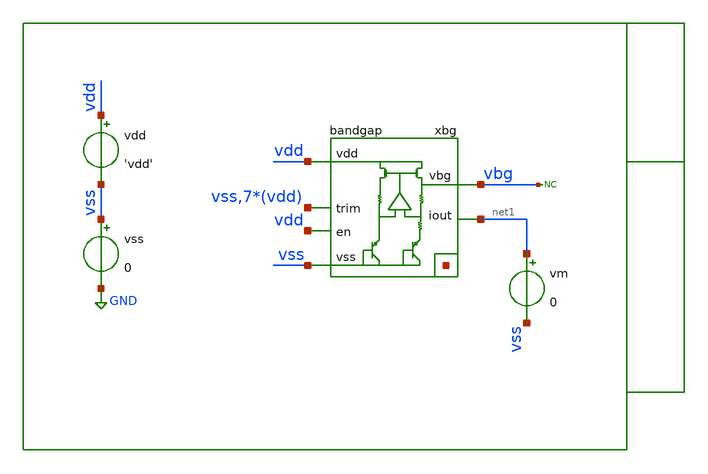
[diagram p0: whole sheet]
** sch_path: xschem/tb/bandgap_cm/bandgap/op_bandgap.sch
**.subckt op_bandgap
xbg vdd vbg vss net2[7] net2[6] net2[5] net2[4] net2[3] net2[2] net2[1] net2[0] vss vdd vdd vdd vdd
+ vdd vdd vdd net1 vdd bandgap
vdd vdd vss 'vdd'
vss vss GND 0
* noconn vbg
vm net1 vss 0
**** begin user architecture code

* Control

.param vdd = 3.3

.temp = 27

.options reltol  = 1e-6
.options abstol  = 1e-12
.options gmin    = 1e-15

*------------------------------------------------------------
* Nodeset for better convergence
*------------------------------------------------------------
.nodeset v(vbg)  = '1'
.nodeset v(xbg.gate) = 'vdd/2'
.nodeset v(xbg.vx)   = '0.70'
.nodeset v(xbg.vbe2) = '0.65'
.nodeset v(xbg.vs1)  = '0'
*------------------------------------------------------------


.control

save all

* optran 0 0 0 100n 0.3m 0
op

let gm_xbg_xm2 = @m.xbg.xm2.m0[gm]
let gm_xbg_xms1 = @m.xbg.xms1.m0[gm]
let gm_xbg_xm1 = @m.xbg.xm1.m0[gm]
let gm_xbg_xmo1 = @m.xbg.xmo1.m0[gm]
let gm_xbg_xmb1 = @m.xbg.xmb1.m0[gm]
let gm_xbg_xmb2 = @m.xbg.xmb2.m0[gm]
let gm_xbg_xmb3 = @m.xbg.xmb3.m0[gm]
let gm_xbg_xmb2 = @m.xbg.xmb2.m0[gm]
let gm_xbg_xmb3 = @m.xbg.xmb3.m0[gm]
let gm_xbg_xmo2 = @m.xbg.xmo2.m0[gm]
let gm_xbg_xme1 = @m.xbg.xme1.m0[gm]
let gm_xbg_xme2 = @m.xbg.xme2.m0[gm]
let gm_xbg_xmi2 = @m.xbg.xmi2.m0[gm]
let gm_xbg_xmi1 = @m.xbg.xmi1.m0[gm]
let gm_xbg_xme3 = @m.xbg.xme3.m0[gm]
let gm_xbg_xme4 = @m.xbg.xme4.m0[gm]
let gm_xbg_xms2 = @m.xbg.xms2.m0[gm]
let gm_xbg_xms3 = @m.xbg.xms3.m0[gm]
let gm_xbg_xms4 = @m.xbg.xms4.m0[gm]
let gm_xamp_xmb1 = @m.xbg.xamp.xmb1.m0[gm]
let gm_xamp_xmb3 = @m.xbg.xamp.xmb3.m0[gm]
let gm_xamp_xmb2 = @m.xbg.xamp.xmb2.m0[gm]
let gm_xamp_xmd1 = @m.xbg.xamp.xmd1.m0[gm]
let gm_xamp_xmb4 = @m.xbg.xamp.xmb4.m0[gm]
let gm_xamp_xmb5 = @m.xbg.xamp.xmb5.m0[gm]
let gm_xamp_xmd2 = @m.xbg.xamp.xmd2.m0[gm]
let gm_xamp_xmt1 = @m.xbg.xamp.xmt1.m0[gm]
let gm_xamp_xmc7 = @m.xbg.xamp.xmc7.m0[gm]
let gm_xamp_xmc8 = @m.xbg.xamp.xmc8.m0[gm]
let gm_xamp_xmc1 = @m.xbg.xamp.xmc1.m0[gm]
let gm_xamp_xmc2 = @m.xbg.xamp.xmc2.m0[gm]
let gm_xamp_xmc3 = @m.xbg.xamp.xmc3.m0[gm]
let gm_xamp_xmc4 = @m.xbg.xamp.xmc4.m0[gm]
let gm_xamp_xmc5 = @m.xbg.xamp.xmc5.m0[gm]
let gm_xamp_xmc6 = @m.xbg.xamp.xmc6.m0[gm]
let gds_xbg_xm2 = @m.xbg.xm2.m0[gds]
let gds_xbg_xms1 = @m.xbg.xms1.m0[gds]
let gds_xbg_xm1 = @m.xbg.xm1.m0[gds]
let gds_xbg_xmo1 = @m.xbg.xmo1.m0[gds]
let gds_xbg_xmb1 = @m.xbg.xmb1.m0[gds]
let gds_xbg_xmb2 = @m.xbg.xmb2.m0[gds]
let gds_xbg_xmb3 = @m.xbg.xmb3.m0[gds]
let gds_xbg_xmb2 = @m.xbg.xmb2.m0[gds]
let gds_xbg_xmb3 = @m.xbg.xmb3.m0[gds]
let gds_xbg_xmo2 = @m.xbg.xmo2.m0[gds]
let gds_xbg_xme1 = @m.xbg.xme1.m0[gds]
let gds_xbg_xme2 = @m.xbg.xme2.m0[gds]
let gds_xbg_xmi2 = @m.xbg.xmi2.m0[gds]
let gds_xbg_xmi1 = @m.xbg.xmi1.m0[gds]
let gds_xbg_xme3 = @m.xbg.xme3.m0[gds]
let gds_xbg_xme4 = @m.xbg.xme4.m0[gds]
let gds_xbg_xms2 = @m.xbg.xms2.m0[gds]
let gds_xbg_xms3 = @m.xbg.xms3.m0[gds]
let gds_xbg_xms4 = @m.xbg.xms4.m0[gds]
let gds_xamp_xmb1 = @m.xbg.xamp.xmb1.m0[gds]
let gds_xamp_xmb3 = @m.xbg.xamp.xmb3.m0[gds]
let gds_xamp_xmb2 = @m.xbg.xamp.xmb2.m0[gds]
let gds_xamp_xmd1 = @m.xbg.xamp.xmd1.m0[gds]
let gds_xamp_xmb4 = @m.xbg.xamp.xmb4.m0[gds]
let gds_xamp_xmb5 = @m.xbg.xamp.xmb5.m0[gds]
let gds_xamp_xmd2 = @m.xbg.xamp.xmd2.m0[gds]
let gds_xamp_xmt1 = @m.xbg.xamp.xmt1.m0[gds]
let gds_xamp_xmc7 = @m.xbg.xamp.xmc7.m0[gds]
let gds_xamp_xmc8 = @m.xbg.xamp.xmc8.m0[gds]
let gds_xamp_xmc1 = @m.xbg.xamp.xmc1.m0[gds]
let gds_xamp_xmc2 = @m.xbg.xamp.xmc2.m0[gds]
let gds_xamp_xmc3 = @m.xbg.xamp.xmc3.m0[gds]
let gds_xamp_xmc4 = @m.xbg.xamp.xmc4.m0[gds]
let gds_xamp_xmc5 = @m.xbg.xamp.xmc5.m0[gds]
let gds_xamp_xmc6 = @m.xbg.xamp.xmc6.m0[gds]
let vdsat_xbg_xm2 = @m.xbg.xm2.m0[vdsat]
let vdsat_xbg_xms1 = @m.xbg.xms1.m0[vdsat]
let vdsat_xbg_xm1 = @m.xbg.xm1.m0[vdsat]
let vdsat_xbg_xmo1 = @m.xbg.xmo1.m0[vdsat]
let vdsat_xbg_xmb1 = @m.xbg.xmb1.m0[vdsat]
let vdsat_xbg_xmb2 = @m.xbg.xmb2.m0[vdsat]
let vdsat_xbg_xmb3 = @m.xbg.xmb3.m0[vdsat]
let vdsat_xbg_xmb2 = @m.xbg.xmb2.m0[vdsat]
let vdsat_xbg_xmb3 = @m.xbg.xmb3.m0[vdsat]
let vdsat_xbg_xmo2 = @m.xbg.xmo2.m0[vdsat]
let vdsat_xbg_xme1 = @m.xbg.xme1.m0[vdsat]
let vdsat_xbg_xme2 = @m.xbg.xme2.m0[vdsat]
let vdsat_xbg_xmi2 = @m.xbg.xmi2.m0[vdsat]
let vdsat_xbg_xmi1 = @m.xbg.xmi1.m0[vdsat]
let vdsat_xbg_xme3 = @m.xbg.xme3.m0[vdsat]
let vdsat_xbg_xme4 = @m.xbg.xme4.m0[vdsat]
let vdsat_xbg_xms2 = @m.xbg.xms2.m0[vdsat]
let vdsat_xbg_xms3 = @m.xbg.xms3.m0[vdsat]
let vdsat_xbg_xms4 = @m.xbg.xms4.m0[vdsat]
let vdsat_xamp_xmb1 = @m.xbg.xamp.xmb1.m0[vdsat]
let vdsat_xamp_xmb3 = @m.xbg.xamp.xmb3.m0[vdsat]
let vdsat_xamp_xmb2 = @m.xbg.xamp.xmb2.m0[vdsat]
let vdsat_xamp_xmd1 = @m.xbg.xamp.xmd1.m0[vdsat]
let vdsat_xamp_xmb4 = @m.xbg.xamp.xmb4.m0[vdsat]
let vdsat_xamp_xmb5 = @m.xbg.xamp.xmb5.m0[vdsat]
let vdsat_xamp_xmd2 = @m.xbg.xamp.xmd2.m0[vdsat]
let vdsat_xamp_xmt1 = @m.xbg.xamp.xmt1.m0[vdsat]
let vdsat_xamp_xmc7 = @m.xbg.xamp.xmc7.m0[vdsat]
let vdsat_xamp_xmc8 = @m.xbg.xamp.xmc8.m0[vdsat]
let vdsat_xamp_xmc1 = @m.xbg.xamp.xmc1.m0[vdsat]
let vdsat_xamp_xmc2 = @m.xbg.xamp.xmc2.m0[vdsat]
let vdsat_xamp_xmc3 = @m.xbg.xamp.xmc3.m0[vdsat]
let vdsat_xamp_xmc4 = @m.xbg.xamp.xmc4.m0[vdsat]
let vdsat_xamp_xmc5 = @m.xbg.xamp.xmc5.m0[vdsat]
let vdsat_xamp_xmc6 = @m.xbg.xamp.xmc6.m0[vdsat]
let vth_xbg_xm2 = @m.xbg.xm2.m0[vth]
let vth_xbg_xms1 = @m.xbg.xms1.m0[vth]
let vth_xbg_xm1 = @m.xbg.xm1.m0[vth]
let vth_xbg_xmo1 = @m.xbg.xmo1.m0[vth]
let vth_xbg_xmb1 = @m.xbg.xmb1.m0[vth]
let vth_xbg_xmb2 = @m.xbg.xmb2.m0[vth]
let vth_xbg_xmb3 = @m.xbg.xmb3.m0[vth]
let vth_xbg_xmb2 = @m.xbg.xmb2.m0[vth]
let vth_xbg_xmb3 = @m.xbg.xmb3.m0[vth]
let vth_xbg_xmo2 = @m.xbg.xmo2.m0[vth]
let vth_xbg_xme1 = @m.xbg.xme1.m0[vth]
let vth_xbg_xme2 = @m.xbg.xme2.m0[vth]
let vth_xbg_xmi2 = @m.xbg.xmi2.m0[vth]
let vth_xbg_xmi1 = @m.xbg.xmi1.m0[vth]
let vth_xbg_xme3 = @m.xbg.xme3.m0[vth]
let vth_xbg_xme4 = @m.xbg.xme4.m0[vth]
let vth_xbg_xms2 = @m.xbg.xms2.m0[vth]
let vth_xbg_xms3 = @m.xbg.xms3.m0[vth]
let vth_xbg_xms4 = @m.xbg.xms4.m0[vth]
let vth_xamp_xmb1 = @m.xbg.xamp.xmb1.m0[vth]
let vth_xamp_xmb3 = @m.xbg.xamp.xmb3.m0[vth]
let vth_xamp_xmb2 = @m.xbg.xamp.xmb2.m0[vth]
let vth_xamp_xmd1 = @m.xbg.xamp.xmd1.m0[vth]
let vth_xamp_xmb4 = @m.xbg.xamp.xmb4.m0[vth]
let vth_xamp_xmb5 = @m.xbg.xamp.xmb5.m0[vth]
let vth_xamp_xmd2 = @m.xbg.xamp.xmd2.m0[vth]
let vth_xamp_xmt1 = @m.xbg.xamp.xmt1.m0[vth]
let vth_xamp_xmc7 = @m.xbg.xamp.xmc7.m0[vth]
let vth_xamp_xmc8 = @m.xbg.xamp.xmc8.m0[vth]
let vth_xamp_xmc1 = @m.xbg.xamp.xmc1.m0[vth]
let vth_xamp_xmc2 = @m.xbg.xamp.xmc2.m0[vth]
let vth_xamp_xmc3 = @m.xbg.xamp.xmc3.m0[vth]
let vth_xamp_xmc4 = @m.xbg.xamp.xmc4.m0[vth]
let vth_xamp_xmc5 = @m.xbg.xamp.xmc5.m0[vth]
let vth_xamp_xmc6 = @m.xbg.xamp.xmc6.m0[vth]
let id_xbg_xm2 = @m.xbg.xm2.m0[id]
let id_xbg_xms1 = @m.xbg.xms1.m0[id]
let id_xbg_xm1 = @m.xbg.xm1.m0[id]
let id_xbg_xmo1 = @m.xbg.xmo1.m0[id]
let id_xbg_xmb1 = @m.xbg.xmb1.m0[id]
let id_xbg_xmb2 = @m.xbg.xmb2.m0[id]
let id_xbg_xmb3 = @m.xbg.xmb3.m0[id]
let id_xbg_xmb2 = @m.xbg.xmb2.m0[id]
let id_xbg_xmb3 = @m.xbg.xmb3.m0[id]
let id_xbg_xmo2 = @m.xbg.xmo2.m0[id]
let id_xbg_xme1 = @m.xbg.xme1.m0[id]
let id_xbg_xme2 = @m.xbg.xme2.m0[id]
let id_xbg_xmi2 = @m.xbg.xmi2.m0[id]
let id_xbg_xmi1 = @m.xbg.xmi1.m0[id]
let id_xbg_xme3 = @m.xbg.xme3.m0[id]
let id_xbg_xme4 = @m.xbg.xme4.m0[id]
let id_xbg_xms2 = @m.xbg.xms2.m0[id]
let id_xbg_xms3 = @m.xbg.xms3.m0[id]
let id_xbg_xms4 = @m.xbg.xms4.m0[id]
let id_xamp_xmb1 = @m.xbg.xamp.xmb1.m0[id]
let id_xamp_xmb3 = @m.xbg.xamp.xmb3.m0[id]
let id_xamp_xmb2 = @m.xbg.xamp.xmb2.m0[id]
let id_xamp_xmd1 = @m.xbg.xamp.xmd1.m0[id]
let id_xamp_xmb4 = @m.xbg.xamp.xmb4.m0[id]
let id_xamp_xmb5 = @m.xbg.xamp.xmb5.m0[id]
let id_xamp_xmd2 = @m.xbg.xamp.xmd2.m0[id]
let id_xamp_xmt1 = @m.xbg.xamp.xmt1.m0[id]
let id_xamp_xmc7 = @m.xbg.xamp.xmc7.m0[id]
let id_xamp_xmc8 = @m.xbg.xamp.xmc8.m0[id]
let id_xamp_xmc1 = @m.xbg.xamp.xmc1.m0[id]
let id_xamp_xmc2 = @m.xbg.xamp.xmc2.m0[id]
let id_xamp_xmc3 = @m.xbg.xamp.xmc3.m0[id]
let id_xamp_xmc4 = @m.xbg.xamp.xmc4.m0[id]
let id_xamp_xmc5 = @m.xbg.xamp.xmc5.m0[id]
let id_xamp_xmc6 = @m.xbg.xamp.xmc6.m0[id]
let vgs_xbg_xm2 = @m.xbg.xm2.m0[vgs]
let vgs_xbg_xms1 = @m.xbg.xms1.m0[vgs]
let vgs_xbg_xm1 = @m.xbg.xm1.m0[vgs]
let vgs_xbg_xmo1 = @m.xbg.xmo1.m0[vgs]
let vgs_xbg_xmb1 = @m.xbg.xmb1.m0[vgs]
let vgs_xbg_xmb2 = @m.xbg.xmb2.m0[vgs]
let vgs_xbg_xmb3 = @m.xbg.xmb3.m0[vgs]
let vgs_xbg_xmb2 = @m.xbg.xmb2.m0[vgs]
let vgs_xbg_xmb3 = @m.xbg.xmb3.m0[vgs]
let vgs_xbg_xmo2 = @m.xbg.xmo2.m0[vgs]
let vgs_xbg_xme1 = @m.xbg.xme1.m0[vgs]
let vgs_xbg_xme2 = @m.xbg.xme2.m0[vgs]
let vgs_xbg_xmi2 = @m.xbg.xmi2.m0[vgs]
let vgs_xbg_xmi1 = @m.xbg.xmi1.m0[vgs]
let vgs_xbg_xme3 = @m.xbg.xme3.m0[vgs]
let vgs_xbg_xme4 = @m.xbg.xme4.m0[vgs]
let vgs_xbg_xms2 = @m.xbg.xms2.m0[vgs]
let vgs_xbg_xms3 = @m.xbg.xms3.m0[vgs]
let vgs_xbg_xms4 = @m.xbg.xms4.m0[vgs]
let vgs_xamp_xmb1 = @m.xbg.xamp.xmb1.m0[vgs]
let vgs_xamp_xmb3 = @m.xbg.xamp.xmb3.m0[vgs]
let vgs_xamp_xmb2 = @m.xbg.xamp.xmb2.m0[vgs]
let vgs_xamp_xmd1 = @m.xbg.xamp.xmd1.m0[vgs]
let vgs_xamp_xmb4 = @m.xbg.xamp.xmb4.m0[vgs]
let vgs_xamp_xmb5 = @m.xbg.xamp.xmb5.m0[vgs]
let vgs_xamp_xmd2 = @m.xbg.xamp.xmd2.m0[vgs]
let vgs_xamp_xmt1 = @m.xbg.xamp.xmt1.m0[vgs]
let vgs_xamp_xmc7 = @m.xbg.xamp.xmc7.m0[vgs]
let vgs_xamp_xmc8 = @m.xbg.xamp.xmc8.m0[vgs]
let vgs_xamp_xmc1 = @m.xbg.xamp.xmc1.m0[vgs]
let vgs_xamp_xmc2 = @m.xbg.xamp.xmc2.m0[vgs]
let vgs_xamp_xmc3 = @m.xbg.xamp.xmc3.m0[vgs]
let vgs_xamp_xmc4 = @m.xbg.xamp.xmc4.m0[vgs]
let vgs_xamp_xmc5 = @m.xbg.xamp.xmc5.m0[vgs]
let vgs_xamp_xmc6 = @m.xbg.xamp.xmc6.m0[vgs]
let vds_xbg_xm2 = @m.xbg.xm2.m0[vds]
let vds_xbg_xms1 = @m.xbg.xms1.m0[vds]
let vds_xbg_xm1 = @m.xbg.xm1.m0[vds]
let vds_xbg_xmo1 = @m.xbg.xmo1.m0[vds]
let vds_xbg_xmb1 = @m.xbg.xmb1.m0[vds]
let vds_xbg_xmb2 = @m.xbg.xmb2.m0[vds]
let vds_xbg_xmb3 = @m.xbg.xmb3.m0[vds]
let vds_xbg_xmb2 = @m.xbg.xmb2.m0[vds]
let vds_xbg_xmb3 = @m.xbg.xmb3.m0[vds]
let vds_xbg_xmo2 = @m.xbg.xmo2.m0[vds]
let vds_xbg_xme1 = @m.xbg.xme1.m0[vds]
let vds_xbg_xme2 = @m.xbg.xme2.m0[vds]
let vds_xbg_xmi2 = @m.xbg.xmi2.m0[vds]
let vds_xbg_xmi1 = @m.xbg.xmi1.m0[vds]
let vds_xbg_xme3 = @m.xbg.xme3.m0[vds]
let vds_xbg_xme4 = @m.xbg.xme4.m0[vds]
let vds_xbg_xms2 = @m.xbg.xms2.m0[vds]
let vds_xbg_xms3 = @m.xbg.xms3.m0[vds]
let vds_xbg_xms4 = @m.xbg.xms4.m0[vds]
let vds_xamp_xmb1 = @m.xbg.xamp.xmb1.m0[vds]
let vds_xamp_xmb3 = @m.xbg.xamp.xmb3.m0[vds]
let vds_xamp_xmb2 = @m.xbg.xamp.xmb2.m0[vds]
let vds_xamp_xmd1 = @m.xbg.xamp.xmd1.m0[vds]
let vds_xamp_xmb4 = @m.xbg.xamp.xmb4.m0[vds]
let vds_xamp_xmb5 = @m.xbg.xamp.xmb5.m0[vds]
let vds_xamp_xmd2 = @m.xbg.xamp.xmd2.m0[vds]
let vds_xamp_xmt1 = @m.xbg.xamp.xmt1.m0[vds]
let vds_xamp_xmc7 = @m.xbg.xamp.xmc7.m0[vds]
let vds_xamp_xmc8 = @m.xbg.xamp.xmc8.m0[vds]
let vds_xamp_xmc1 = @m.xbg.xamp.xmc1.m0[vds]
let vds_xamp_xmc2 = @m.xbg.xamp.xmc2.m0[vds]
let vds_xamp_xmc3 = @m.xbg.xamp.xmc3.m0[vds]
let vds_xamp_xmc4 = @m.xbg.xamp.xmc4.m0[vds]
let vds_xamp_xmc5 = @m.xbg.xamp.xmc5.m0[vds]
let vds_xamp_xmc6 = @m.xbg.xamp.xmc6.m0[vds]

let vsat_xbg_xm2  = vds_xbg_xm2  - vdsat_xbg_xm2
let vsat_xbg_xms1 = vds_xbg_xms1 - vdsat_xbg_xms1
let vsat_xbg_xm1  = vds_xbg_xm1  - vdsat_xbg_xm1
let vsat_xbg_xmo1 = vds_xbg_xmo1 - vdsat_xbg_xmo1
let vsat_xbg_xmb1 = vds_xbg_xmb1 - vdsat_xbg_xmb1
let vsat_xbg_xmb2 = vds_xbg_xmb2 - vdsat_xbg_xmb2
let vsat_xbg_xmb3 = vds_xbg_xmb3 - vdsat_xbg_xmb3
let vsat_xbg_xmb2 = vds_xbg_xmb2 - vdsat_xbg_xmb2
let vsat_xbg_xmb3 = vds_xbg_xmb3 - vdsat_xbg_xmb3
let vsat_xbg_xmo2 = vds_xbg_xmo2 - vdsat_xbg_xmo2
let vsat_xbg_xme1 = vds_xbg_xme1 - vdsat_xbg_xme1
let vsat_xbg_xme2 = vds_xbg_xme2 - vdsat_xbg_xme2
let vsat_xbg_xmi2 = vds_xbg_xmi2 - vdsat_xbg_xmi2
let vsat_xbg_xmi1 = vds_xbg_xmi1 - vdsat_xbg_xmi1
let vsat_xbg_xme3 = vds_xbg_xme3 - vdsat_xbg_xme3
let vsat_xbg_xme4 = vds_xbg_xme4 - vdsat_xbg_xme4
let vsat_xbg_xms2 = vds_xbg_xms2 - vdsat_xbg_xms2
let vsat_xbg_xms3 = vds_xbg_xms3 - vdsat_xbg_xms3
let vsat_xbg_xms4 = vds_xbg_xms4 - vdsat_xbg_xms4
let vsat_xamp_xmb1 = vds_xamp_xmb1 - vdsat_xamp_xmb1
let vsat_xamp_xmb3 = vds_xamp_xmb3 - vdsat_xamp_xmb3
let vsat_xamp_xmb2 = vds_xamp_xmb2 - vdsat_xamp_xmb2
let vsat_xamp_xmd1 = vds_xamp_xmd1 - vdsat_xamp_xmd1
let vsat_xamp_xmb4 = vds_xamp_xmb4 - vdsat_xamp_xmb4
let vsat_xamp_xmb5 = vds_xamp_xmb5 - vdsat_xamp_xmb5
let vsat_xamp_xmd2 = vds_xamp_xmd2 - vdsat_xamp_xmd2
let vsat_xamp_xmt1 = vds_xamp_xmt1 - vdsat_xamp_xmt1
let vsat_xamp_xmc7 = vds_xamp_xmc7 - vdsat_xamp_xmc7
let vsat_xamp_xmc8 = vds_xamp_xmc8 - vdsat_xamp_xmc8
let vsat_xamp_xmc1 = vds_xamp_xmc1 - vdsat_xamp_xmc1
let vsat_xamp_xmc2 = vds_xamp_xmc2 - vdsat_xamp_xmc2
let vsat_xamp_xmc3 = vds_xamp_xmc3 - vdsat_xamp_xmc3
let vsat_xamp_xmc4 = vds_xamp_xmc4 - vdsat_xamp_xmc4
let vsat_xamp_xmc5 = vds_xamp_xmc5 - vdsat_xamp_xmc5
let vsat_xamp_xmc6 = vds_xamp_xmc6 - vdsat_xamp_xmc6

let vov_xbg_xm2  = vgs_xbg_xm2  - vth_xbg_xm2
let vov_xbg_xms1 = vgs_xbg_xms1 - vth_xbg_xms1
let vov_xbg_xm1  = vgs_xbg_xm1  - vth_xbg_xm1
let vov_xbg_xmo1 = vgs_xbg_xmo1 - vth_xbg_xmo1
let vov_xbg_xmb1 = vgs_xbg_xmb1 - vth_xbg_xmb1
let vov_xbg_xmb2 = vgs_xbg_xmb2 - vth_xbg_xmb2
let vov_xbg_xmb3 = vgs_xbg_xmb3 - vth_xbg_xmb3
let vov_xbg_xmb2 = vgs_xbg_xmb2 - vth_xbg_xmb2
let vov_xbg_xmb3 = vgs_xbg_xmb3 - vth_xbg_xmb3
let vov_xbg_xmo2 = vgs_xbg_xmo2 - vth_xbg_xmo2
let vov_xbg_xme1 = vgs_xbg_xme1 - vth_xbg_xme1
let vov_xbg_xme2 = vgs_xbg_xme2 - vth_xbg_xme2
let vov_xbg_xmi2 = vgs_xbg_xmi2 - vth_xbg_xmi2
let vov_xbg_xmi1 = vgs_xbg_xmi1 - vth_xbg_xmi1
let vov_xbg_xme3 = vgs_xbg_xme3 - vth_xbg_xme3
let vov_xbg_xme4 = vgs_xbg_xme4 - vth_xbg_xme4
let vov_xbg_xms2 = vgs_xbg_xms2 - vth_xbg_xms2
let vov_xbg_xms3 = vgs_xbg_xms3 - vth_xbg_xms3
let vov_xbg_xms4 = vgs_xbg_xms4 - vth_xbg_xms4
let vov_xamp_xmb1 = vgs_xamp_xmb1 - vth_xamp_xmb1
let vov_xamp_xmb3 = vgs_xamp_xmb3 - vth_xamp_xmb3
let vov_xamp_xmb2 = vgs_xamp_xmb2 - vth_xamp_xmb2
let vov_xamp_xmd1 = vgs_xamp_xmd1 - vth_xamp_xmd1
let vov_xamp_xmb4 = vgs_xamp_xmb4 - vth_xamp_xmb4
let vov_xamp_xmb5 = vgs_xamp_xmb5 - vth_xamp_xmb5
let vov_xamp_xmd2 = vgs_xamp_xmd2 - vth_xamp_xmd2
let vov_xamp_xmt1 = vgs_xamp_xmt1 - vth_xamp_xmt1
let vov_xamp_xmc7 = vgs_xamp_xmc7 - vth_xamp_xmc7
let vov_xamp_xmc8 = vgs_xamp_xmc8 - vth_xamp_xmc8
let vov_xamp_xmc1 = vgs_xamp_xmc1 - vth_xamp_xmc1
let vov_xamp_xmc2 = vgs_xamp_xmc2 - vth_xamp_xmc2
let vov_xamp_xmc3 = vgs_xamp_xmc3 - vth_xamp_xmc3
let vov_xamp_xmc4 = vgs_xamp_xmc4 - vth_xamp_xmc4
let vov_xamp_xmc5 = vgs_xamp_xmc5 - vth_xamp_xmc5
let vov_xamp_xmc6 = vgs_xamp_xmc6 - vth_xamp_xmc6



let ie_xq1 = abs(v.xbg.vmbjt1#branch)
let ie_xq2 = abs(v.xbg.vmbjt2#branch)
let i_amp = abs(v.xbg.vmamp#branch)
let i_xm1 = abs(v.xbg.vmxm1#branch)
let i_xm2 = abs(v.xbg.vmxm2#branch)
let i_r1 = ie_xq2
let i_r3 = abs(v.xbg.vmr3#branch)
let i_r2 = abs(v.xbg.vmr2#branch)
let iout = abs(vm#branch)

print vbg
print iout

write op_bandgap.raw

.endc
.end


 * Model Corners

.include $::CORNERS/ngspice/tt.spice
*.include $::CORNERS/ngspice/ff.spice
*.include $::CORNERS/ngspice/ss.spice
*.include $::CORNERS/ngspice/sf.spice
*.include $::CORNERS/ngspice/fs.spice

 * extract

* tb_amplifier pex
*.include $::DESIGN_PATH/sch/bandgap_cm/bg_amplifier/bg_amplifier.pex.spice

* bandgap pex
*.include $::DESIGN_PATH/sch/bandgap_cm/bandgap/bandgap.pex.spice

**** end user architecture code
**.ends
.GLOBAL GND
.end
